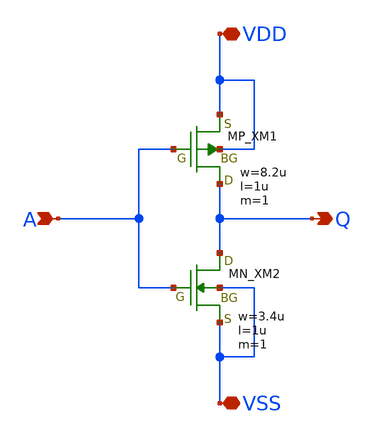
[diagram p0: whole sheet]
** sch_path: inverter/inverter_Satoshi_Kawakami.sch
**.subckt inverter_Satoshi_Kawakami A Q VDD VSS
*.ipin A
*.opin Q
*.iopin VDD
*.iopin VSS
XXM1 Q A VDD VDD PMOS w=8.2u l=1u nrd=0 nrs=0 m=1
XXM2 Q A VSS VSS NMOS w=3.4u l=1u nrd=0 nrs=0 m=1
**.ends
.end
